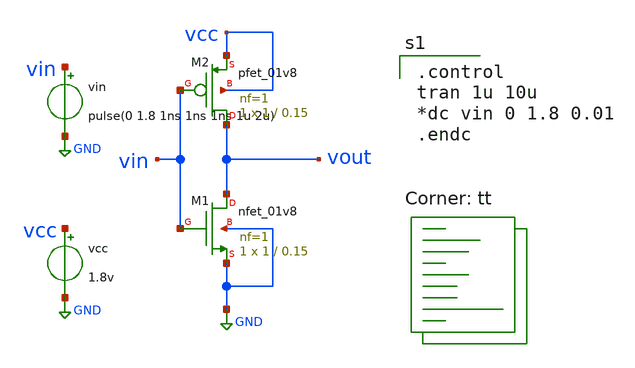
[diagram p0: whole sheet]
** sch_path: inverter_new.sch
**.subckt inverter_new
vin vin GND pulse(0 1.8 1ns 1ns 1ns 1u 2u)
vcc vcc GND 1.8v
XM1 vout vin GND GND sky130_fd_pr__nfet_01v8 L=0.15 W=1 nf=1 ad='int((nf+1)/2) * W/nf * 0.29' as='int((nf+2)/2) * W/nf * 0.29'
+ pd='2*int((nf+1)/2) * (W/nf + 0.29)' ps='2*int((nf+2)/2) * (W/nf + 0.29)' nrd='0.29 / W' nrs='0.29 / W'
+ sa=0 sb=0 sd=0 mult=1 m=1
XM2 vout vin vcc vcc sky130_fd_pr__pfet_01v8 L=0.15 W=1 nf=1 ad='int((nf+1)/2) * W/nf * 0.29' as='int((nf+2)/2) * W/nf * 0.29'
+ pd='2*int((nf+1)/2) * (W/nf + 0.29)' ps='2*int((nf+2)/2) * (W/nf + 0.29)' nrd='0.29 / W' nrs='0.29 / W'
+ sa=0 sb=0 sd=0 mult=1 m=1
**** begin user architecture code

.control
tran 1u 10u
*dc vin 0 1.8 0.01
.endc

.lib $::SKYWATER_MODELS/sky130.lib.spice tt
**** end user architecture code
**.ends
.GLOBAL GND
.end
